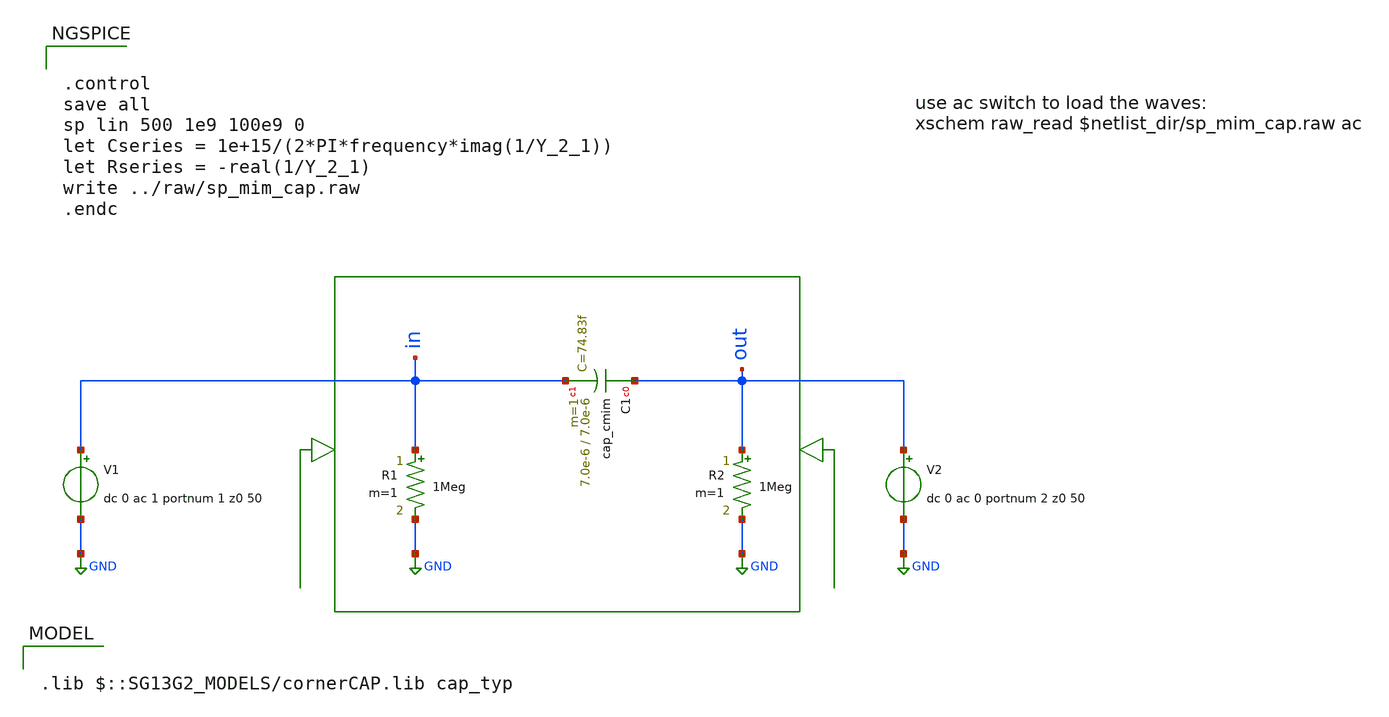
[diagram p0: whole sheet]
** sch_path: ihp-sg13g2/libs.tech/xschem/sg13g2_tests/sp_mim_cap.sch
* Copyright 2021 Stefan Frederik Schippers
* Licensed under the Apache License, Version 2.0 (the "License");
* you may not use this file except in compliance with the License.
* You may obtain a copy of the License at
* https://www.apache.org/licenses/LICENSE-2.0
* Unless required by applicable law or agreed to in writing, software
* distributed under the License is distributed on an "AS IS" BASIS,
* WITHOUT WARRANTIES OR CONDITIONS OF ANY KIND, either express or implied.
* See the License for the specific language governing permissions and
* limitations under the License.
* Copyright 2023 IHP PDK Authors
**.subckt sp_mim_cap
R1 in GND 1Meg m=1
V1 in GND dc 0 ac 1 portnum 1 z0 50
R2 out GND 1Meg m=1
V2 out GND dc 0 ac 0 portnum 2 z0 50
XC1 out in cap_cmim w=7.0e-6 l=7.0e-6 m=1 mm_ok=1
**** begin user architecture code


.control
save all
sp lin 500 1e9 100e9 0
let Cseries = 1e+15/(2*PI*frequency*imag(1/Y_2_1))
let Rseries = -real(1/Y_2_1)
write ../raw/sp_mim_cap.raw
.endc



.lib $::SG13G2_MODELS/cornerCAP.lib cap_typ

**** end user architecture code
**.ends
.GLOBAL GND
.end
